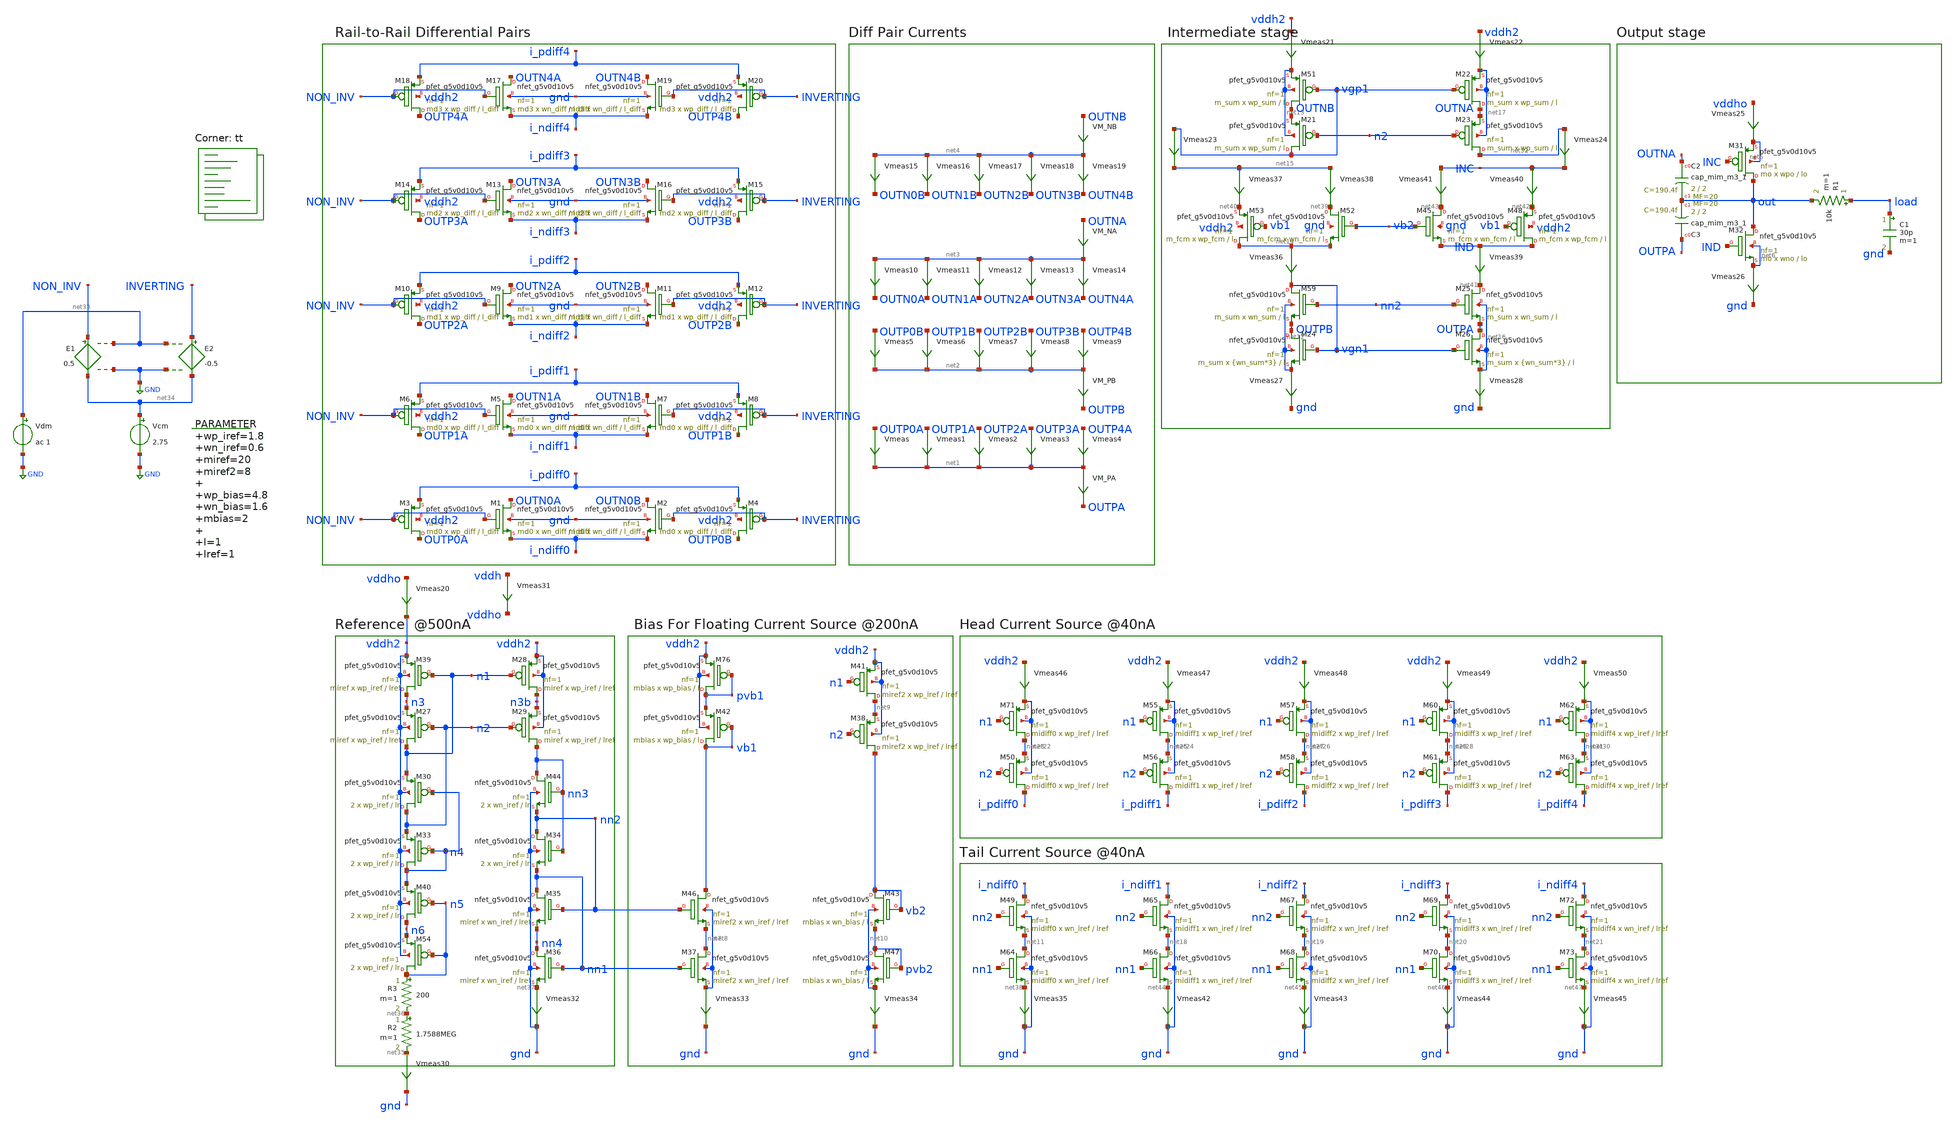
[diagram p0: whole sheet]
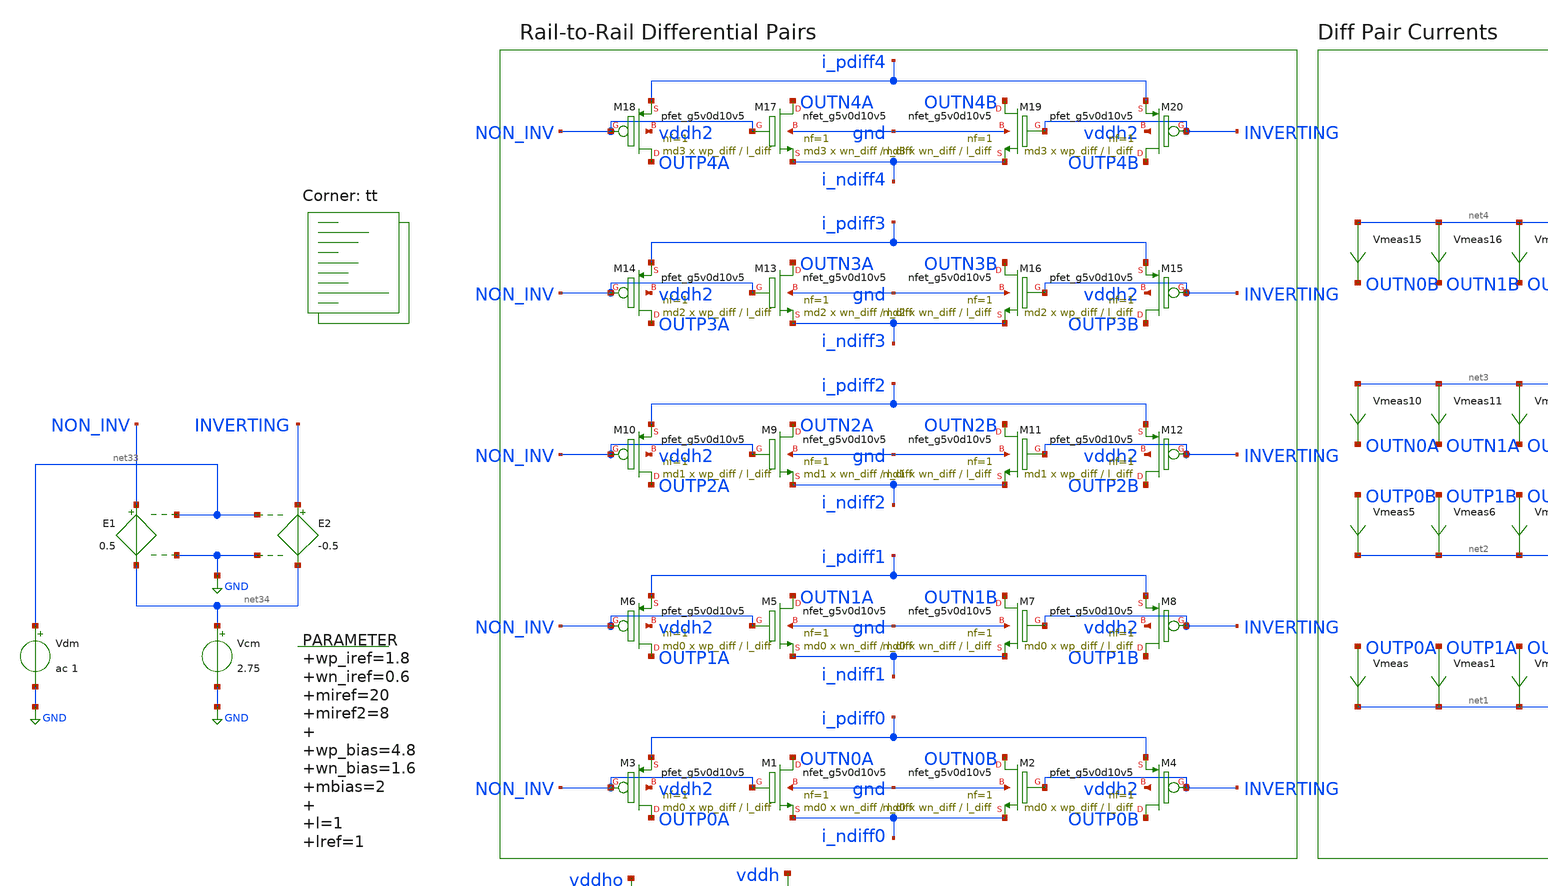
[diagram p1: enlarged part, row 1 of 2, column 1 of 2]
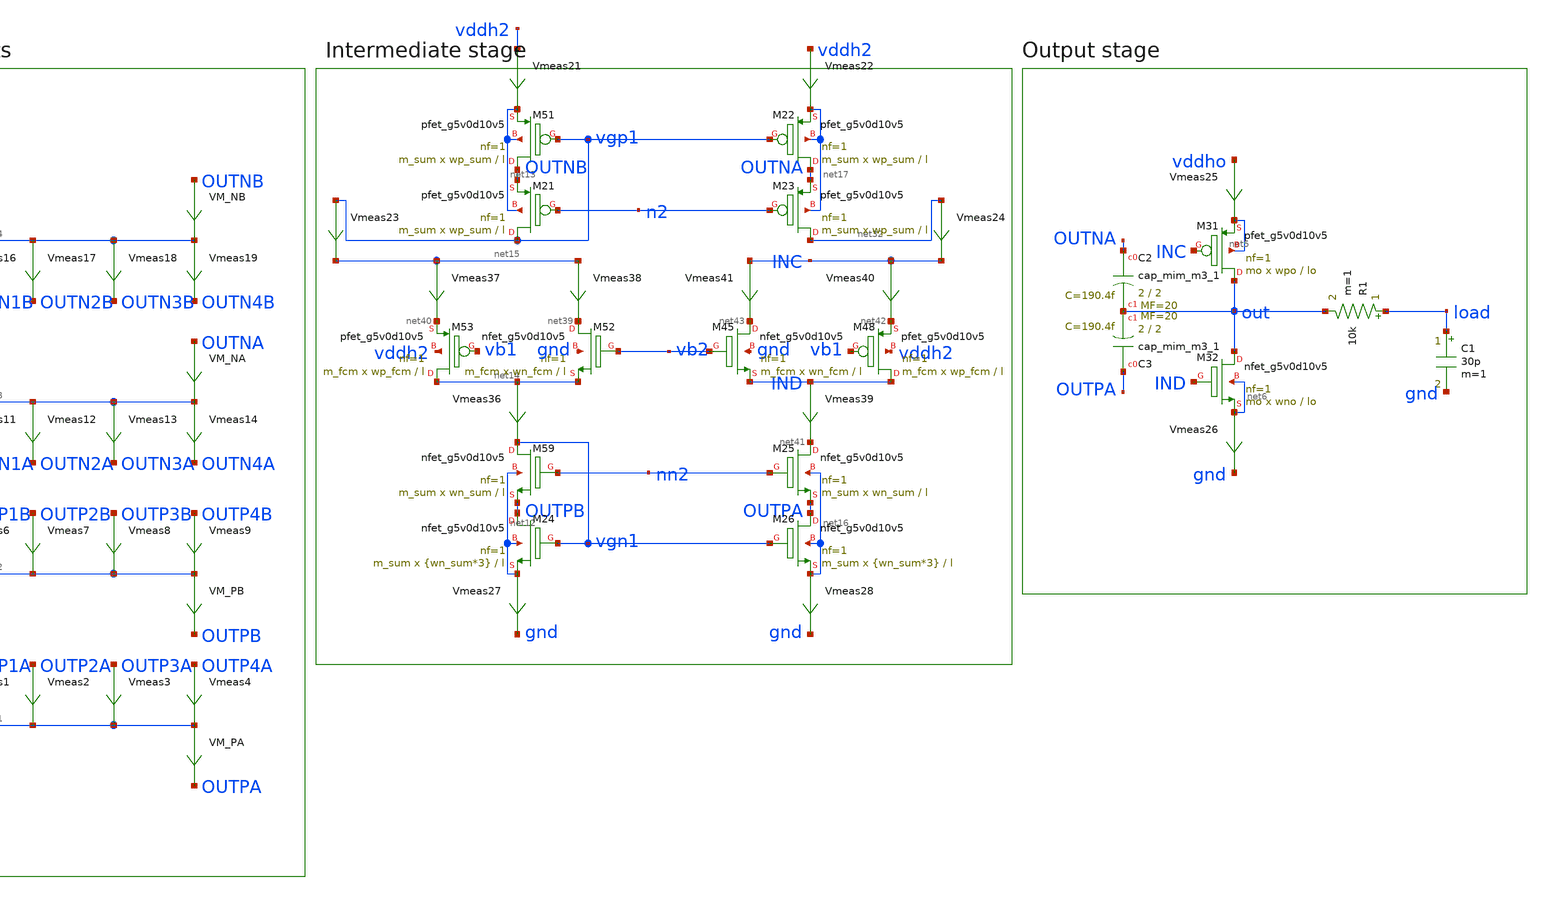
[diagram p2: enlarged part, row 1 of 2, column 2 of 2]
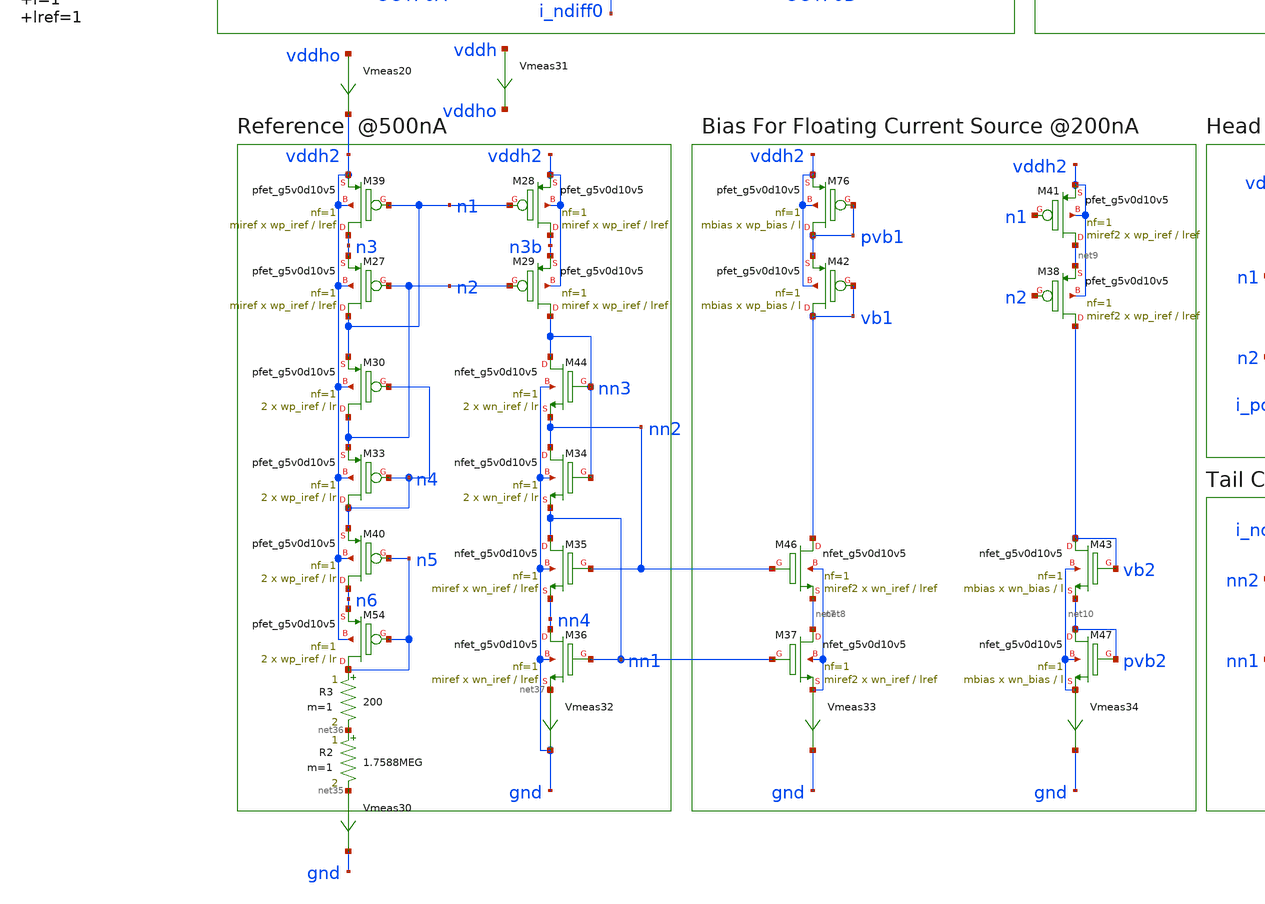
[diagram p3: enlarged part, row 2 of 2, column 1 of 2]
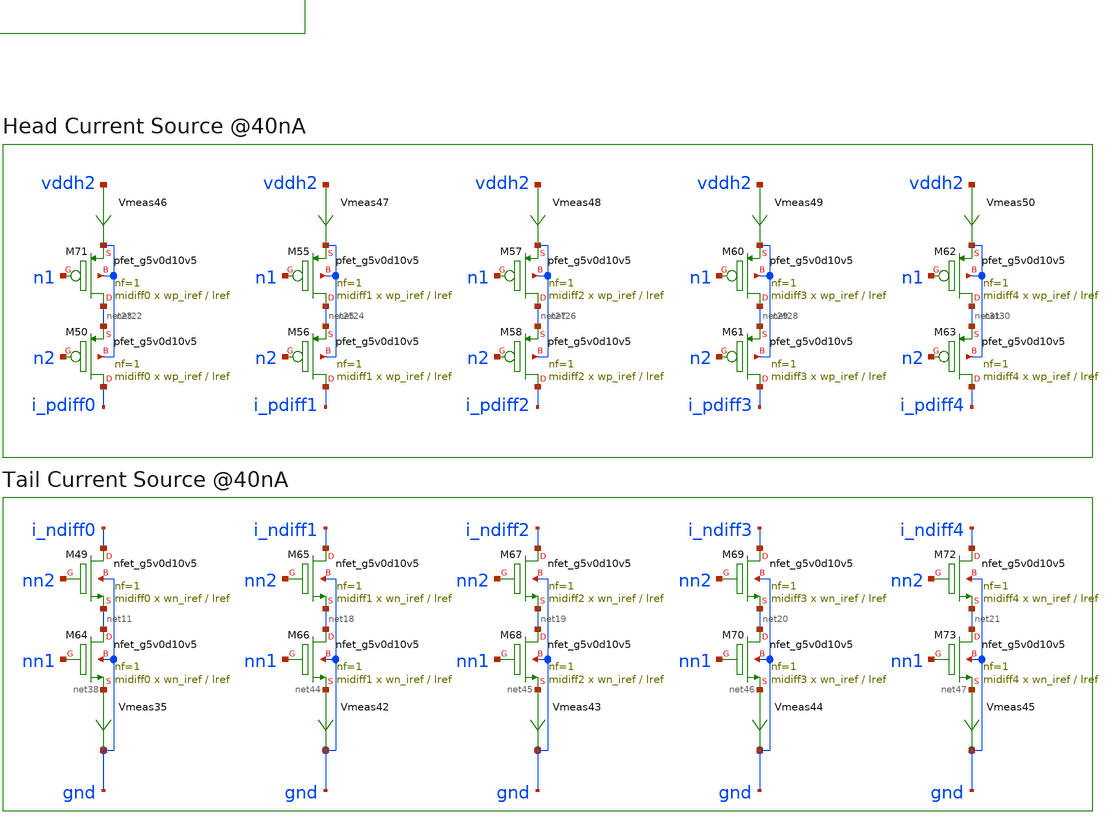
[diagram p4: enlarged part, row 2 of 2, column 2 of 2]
** sch_path: xschem/op_amp_v3-tb.sch
**.subckt op_amp_v3-tb
XM1 OUTN0A NON_INV i_ndiff0 gnd sky130_fd_pr__nfet_g5v0d10v5 L=l_diff W=wn_diff nf=1 ad='int((nf+1)/2) * W/nf * 0.29'
+ as='int((nf+2)/2) * W/nf * 0.29' pd='2*int((nf+1)/2) * (W/nf + 0.29)' ps='2*int((nf+2)/2) * (W/nf + 0.29)'
+ nrd='0.29 / W' nrs='0.29 / W' sa=0 sb=0 sd=0 mult=md0 m=md0
XM3 OUTP0A NON_INV i_pdiff0 vddh2 sky130_fd_pr__pfet_g5v0d10v5 L=l_diff W=wp_diff nf=1 ad='int((nf+1)/2) * W/nf * 0.29'
+ as='int((nf+2)/2) * W/nf * 0.29' pd='2*int((nf+1)/2) * (W/nf + 0.29)' ps='2*int((nf+2)/2) * (W/nf + 0.29)'
+ nrd='0.29 / W' nrs='0.29 / W' sa=0 sb=0 sd=0 mult=md0 m=md0
Vmeas OUTP0A net1 0
.save i(vmeas)
Vmeas1 OUTP1A net1 0
.save i(vmeas1)
Vmeas2 OUTP2A net1 0
.save i(vmeas2)
Vmeas3 OUTP3A net1 0
.save i(vmeas3)
Vmeas4 OUTP4A net1 0
.save i(vmeas4)
Vmeas5 OUTP0B net2 0
.save i(vmeas5)
Vmeas6 OUTP1B net2 0
.save i(vmeas6)
Vmeas7 OUTP2B net2 0
.save i(vmeas7)
Vmeas8 OUTP3B net2 0
.save i(vmeas8)
Vmeas9 OUTP4B net2 0
.save i(vmeas9)
Vmeas10 net3 OUTN0A 0
.save i(vmeas10)
Vmeas11 net3 OUTN1A 0
.save i(vmeas11)
Vmeas12 net3 OUTN2A 0
.save i(vmeas12)
Vmeas13 net3 OUTN3A 0
.save i(vmeas13)
Vmeas14 net3 OUTN4A 0
.save i(vmeas14)
Vmeas15 net4 OUTN0B 0
.save i(vmeas15)
Vmeas16 net4 OUTN1B 0
.save i(vmeas16)
Vmeas17 net4 OUTN2B 0
.save i(vmeas17)
Vmeas18 net4 OUTN3B 0
.save i(vmeas18)
Vmeas19 net4 OUTN4B 0
.save i(vmeas19)
XM31 out INC net5 net5 sky130_fd_pr__pfet_g5v0d10v5 L=lo W=wpo nf=1 ad='int((nf+1)/2) * W/nf * 0.29'
+ as='int((nf+2)/2) * W/nf * 0.29' pd='2*int((nf+1)/2) * (W/nf + 0.29)' ps='2*int((nf+2)/2) * (W/nf + 0.29)'
+ nrd='0.29 / W' nrs='0.29 / W' sa=0 sb=0 sd=0 mult=mo m=mo
XM32 out IND net6 net6 sky130_fd_pr__nfet_g5v0d10v5 L=lo W=wno nf=1 ad='int((nf+1)/2) * W/nf * 0.29'
+ as='int((nf+2)/2) * W/nf * 0.29' pd='2*int((nf+1)/2) * (W/nf + 0.29)' ps='2*int((nf+2)/2) * (W/nf + 0.29)'
+ nrd='0.29 / W' nrs='0.29 / W' sa=0 sb=0 sd=0 mult=mo m=mo
R1 load out 10k m=1
Vmeas25 vddho net5 0
.save i(vmeas25)
Vmeas26 net6 gnd 0
.save i(vmeas26)
C1 load gnd 30p m=1
VM_NB OUTNB net4 0
.save i(vm_nb)
VM_NA OUTNA net3 0
.save i(vm_na)
VM_PB net2 OUTPB 0
.save i(vm_pb)
VM_PA net1 OUTPA 0
.save i(vm_pa)
XM5 OUTN1A NON_INV i_ndiff1 gnd sky130_fd_pr__nfet_g5v0d10v5 L=l_diff W=wn_diff nf=1 ad='int((nf+1)/2) * W/nf * 0.29'
+ as='int((nf+2)/2) * W/nf * 0.29' pd='2*int((nf+1)/2) * (W/nf + 0.29)' ps='2*int((nf+2)/2) * (W/nf + 0.29)'
+ nrd='0.29 / W' nrs='0.29 / W' sa=0 sb=0 sd=0 mult=md0 m=md0
XM6 OUTP1A NON_INV i_pdiff1 vddh2 sky130_fd_pr__pfet_g5v0d10v5 L=l_diff W=wp_diff nf=1 ad='int((nf+1)/2) * W/nf * 0.29'
+ as='int((nf+2)/2) * W/nf * 0.29' pd='2*int((nf+1)/2) * (W/nf + 0.29)' ps='2*int((nf+2)/2) * (W/nf + 0.29)'
+ nrd='0.29 / W' nrs='0.29 / W' sa=0 sb=0 sd=0 mult=md0 m=md0
XM9 OUTN2A NON_INV i_ndiff2 gnd sky130_fd_pr__nfet_g5v0d10v5 L=l_diff W=wn_diff nf=1 ad='int((nf+1)/2) * W/nf * 0.29'
+ as='int((nf+2)/2) * W/nf * 0.29' pd='2*int((nf+1)/2) * (W/nf + 0.29)' ps='2*int((nf+2)/2) * (W/nf + 0.29)'
+ nrd='0.29 / W' nrs='0.29 / W' sa=0 sb=0 sd=0 mult=md1 m=md1
XM10 OUTP2A NON_INV i_pdiff2 vddh2 sky130_fd_pr__pfet_g5v0d10v5 L=l_diff W=wp_diff nf=1 ad='int((nf+1)/2) * W/nf * 0.29'
+ as='int((nf+2)/2) * W/nf * 0.29' pd='2*int((nf+1)/2) * (W/nf + 0.29)' ps='2*int((nf+2)/2) * (W/nf + 0.29)'
+ nrd='0.29 / W' nrs='0.29 / W' sa=0 sb=0 sd=0 mult=md1 m=md1
XM13 OUTN3A NON_INV i_ndiff3 gnd sky130_fd_pr__nfet_g5v0d10v5 L=l_diff W=wn_diff nf=1 ad='int((nf+1)/2) * W/nf * 0.29'
+ as='int((nf+2)/2) * W/nf * 0.29' pd='2*int((nf+1)/2) * (W/nf + 0.29)' ps='2*int((nf+2)/2) * (W/nf + 0.29)'
+ nrd='0.29 / W' nrs='0.29 / W' sa=0 sb=0 sd=0 mult=md2 m=md2
XM14 OUTP3A NON_INV i_pdiff3 vddh2 sky130_fd_pr__pfet_g5v0d10v5 L=l_diff W=wp_diff nf=1 ad='int((nf+1)/2) * W/nf * 0.29'
+ as='int((nf+2)/2) * W/nf * 0.29' pd='2*int((nf+1)/2) * (W/nf + 0.29)' ps='2*int((nf+2)/2) * (W/nf + 0.29)'
+ nrd='0.29 / W' nrs='0.29 / W' sa=0 sb=0 sd=0 mult=md2 m=md2
XM17 OUTN4A NON_INV i_ndiff4 gnd sky130_fd_pr__nfet_g5v0d10v5 L=l_diff W=wn_diff nf=1 ad='int((nf+1)/2) * W/nf * 0.29'
+ as='int((nf+2)/2) * W/nf * 0.29' pd='2*int((nf+1)/2) * (W/nf + 0.29)' ps='2*int((nf+2)/2) * (W/nf + 0.29)'
+ nrd='0.29 / W' nrs='0.29 / W' sa=0 sb=0 sd=0 mult=md3 m=md3
XM18 OUTP4A NON_INV i_pdiff4 vddh2 sky130_fd_pr__pfet_g5v0d10v5 L=l_diff W=wp_diff nf=1 ad='int((nf+1)/2) * W/nf * 0.29'
+ as='int((nf+2)/2) * W/nf * 0.29' pd='2*int((nf+1)/2) * (W/nf + 0.29)' ps='2*int((nf+2)/2) * (W/nf + 0.29)'
+ nrd='0.29 / W' nrs='0.29 / W' sa=0 sb=0 sd=0 mult=md3 m=md3
XM39 n3 n1 vddh2 vddh2 sky130_fd_pr__pfet_g5v0d10v5 L=lref W=wp_iref nf=1 ad='int((nf+1)/2) * W/nf * 0.29'
+ as='int((nf+2)/2) * W/nf * 0.29' pd='2*int((nf+1)/2) * (W/nf + 0.29)' ps='2*int((nf+2)/2) * (W/nf + 0.29)'
+ nrd='0.29 / W' nrs='0.29 / W' sa=0 sb=0 sd=0 mult=miref m=miref
Vmeas30 net35 gnd 0
.save i(vmeas30)
R3 n5 net36 200 m=1
Vmeas31 vddh vddho 0
.save i(vmeas31)
XM44 nn3 nn3 nn2 gnd sky130_fd_pr__nfet_g5v0d10v5 L=lr W=wn_iref nf=1 ad='int((nf+1)/2) * W/nf * 0.29'
+ as='int((nf+2)/2) * W/nf * 0.29' pd='2*int((nf+1)/2) * (W/nf + 0.29)' ps='2*int((nf+2)/2) * (W/nf + 0.29)'
+ nrd='0.29 / W' nrs='0.29 / W' sa=0 sb=0 sd=0 mult=2 m=2
Vmeas32 net37 gnd 0
.save i(vmeas32)
XM46 vb1 nn2 net7 net8 sky130_fd_pr__nfet_g5v0d10v5 L=lref W=wn_iref nf=1 ad='int((nf+1)/2) * W/nf * 0.29'
+ as='int((nf+2)/2) * W/nf * 0.29' pd='2*int((nf+1)/2) * (W/nf + 0.29)' ps='2*int((nf+2)/2) * (W/nf + 0.29)'
+ nrd='0.29 / W' nrs='0.29 / W' sa=0 sb=0 sd=0 mult=miref2 m=miref2
Vmeas33 net8 gnd 0
.save i(vmeas33)
XM47 pvb2 pvb2 net10 net10 sky130_fd_pr__nfet_g5v0d10v5 L=l W=wn_bias nf=1 ad='int((nf+1)/2) * W/nf * 0.29'
+ as='int((nf+2)/2) * W/nf * 0.29' pd='2*int((nf+1)/2) * (W/nf + 0.29)' ps='2*int((nf+2)/2) * (W/nf + 0.29)'
+ nrd='0.29 / W' nrs='0.29 / W' sa=0 sb=0 sd=0 mult=mbias m=mbias
Vmeas34 net10 gnd 0
.save i(vmeas34)
XM49 i_ndiff0 nn2 net11 gnd sky130_fd_pr__nfet_g5v0d10v5 L=lref W=wn_iref nf=1 ad='int((nf+1)/2) * W/nf * 0.29'
+ as='int((nf+2)/2) * W/nf * 0.29' pd='2*int((nf+1)/2) * (W/nf + 0.29)' ps='2*int((nf+2)/2) * (W/nf + 0.29)'
+ nrd='0.29 / W' nrs='0.29 / W' sa=0 sb=0 sd=0 mult=midiff0 m=midiff0
Vmeas35 net38 gnd 0
.save i(vmeas35)
Vmeas36 net14 vgn1 0
.save i(vmeas36)
XM51 OUTNB vgp1 net13 net13 sky130_fd_pr__pfet_g5v0d10v5 L=l W=wp_sum nf=1 ad='int((nf+1)/2) * W/nf * 0.29'
+ as='int((nf+2)/2) * W/nf * 0.29' pd='2*int((nf+1)/2) * (W/nf + 0.29)' ps='2*int((nf+2)/2) * (W/nf + 0.29)'
+ nrd='0.29 / W' nrs='0.29 / W' sa=0 sb=0 sd=0 mult=m_sum m=m_sum
XM52 net39 vb2 net14 gnd sky130_fd_pr__nfet_g5v0d10v5 L=l W=wn_fcm nf=1 ad='int((nf+1)/2) * W/nf * 0.29'
+ as='int((nf+2)/2) * W/nf * 0.29' pd='2*int((nf+1)/2) * (W/nf + 0.29)' ps='2*int((nf+2)/2) * (W/nf + 0.29)'
+ nrd='0.29 / W' nrs='0.29 / W' sa=0 sb=0 sd=0 mult=m_fcm m=m_fcm
Vmeas37 net15 net40 0
.save i(vmeas37)
Vmeas38 net15 net39 0
.save i(vmeas38)
XM53 net14 vb1 net40 vddh2 sky130_fd_pr__pfet_g5v0d10v5 L=l W=wp_fcm nf=1 ad='int((nf+1)/2) * W/nf * 0.29'
+ as='int((nf+2)/2) * W/nf * 0.29' pd='2*int((nf+1)/2) * (W/nf + 0.29)' ps='2*int((nf+2)/2) * (W/nf + 0.29)'
+ nrd='0.29 / W' nrs='0.29 / W' sa=0 sb=0 sd=0 mult=m_fcm m=m_fcm
Vmeas39 IND net41 0
.save i(vmeas39)
Vmeas40 INC net42 0
.save i(vmeas40)
Vmeas41 INC net43 0
.save i(vmeas41)
XM59 vgn1 nn2 OUTPB net12 sky130_fd_pr__nfet_g5v0d10v5 L=l W=wn_sum nf=1 ad='int((nf+1)/2) * W/nf * 0.29'
+ as='int((nf+2)/2) * W/nf * 0.29' pd='2*int((nf+1)/2) * (W/nf + 0.29)' ps='2*int((nf+2)/2) * (W/nf + 0.29)'
+ nrd='0.29 / W' nrs='0.29 / W' sa=0 sb=0 sd=0 mult=m_sum m=m_sum
Vmeas42 net44 gnd 0
.save i(vmeas42)
Vmeas43 net45 gnd 0
.save i(vmeas43)
Vmeas44 net46 gnd 0
.save i(vmeas44)
Vmeas45 net47 gnd 0
.save i(vmeas45)
XM71 net23 n1 net22 net22 sky130_fd_pr__pfet_g5v0d10v5 L=lref W=wp_iref nf=1 ad='int((nf+1)/2) * W/nf * 0.29'
+ as='int((nf+2)/2) * W/nf * 0.29' pd='2*int((nf+1)/2) * (W/nf + 0.29)' ps='2*int((nf+2)/2) * (W/nf + 0.29)'
+ nrd='0.29 / W' nrs='0.29 / W' sa=0 sb=0 sd=0 mult=midiff0 m=midiff0
Vmeas46 vddh2 net22 0
.save i(vmeas46)
XM76 pvb1 pvb1 vddh2 vddh2 sky130_fd_pr__pfet_g5v0d10v5 L=l W=wp_bias nf=1 ad='int((nf+1)/2) * W/nf * 0.29'
+ as='int((nf+2)/2) * W/nf * 0.29' pd='2*int((nf+1)/2) * (W/nf + 0.29)' ps='2*int((nf+2)/2) * (W/nf + 0.29)'
+ nrd='0.29 / W' nrs='0.29 / W' sa=0 sb=0 sd=0 mult=mbias m=mbias
Vmeas47 vddh2 net24 0
.save i(vmeas47)
Vmeas48 vddh2 net26 0
.save i(vmeas48)
Vmeas49 vddh2 net28 0
.save i(vmeas49)
Vmeas50 vddh2 net30 0
.save i(vmeas50)
.param wp_iref=1.8 wn_iref=0.6 miref=20 miref2=8 wp_bias=4.8 wn_bias=1.6 mbias=2 l=1 lref=1 lr=20
+ midiff0=2 midiff1=2 midiff2=4 midiff3=8 midiff4=16 wp_diff=3 wn_diff=1 l_diff=1 wp_sum=4.8 wn_sum=1.6 l_sum=1
+ m_sum=2 wp_fcm=wp_bias wn_fcm=wn_bias m_fcm=2 wpo=6 wno=2 lo=1 mo=2 md0=4 md1=4 md2=4 md3=4

XM21 vgp1 n2 OUTNB net13 sky130_fd_pr__pfet_g5v0d10v5 L=l W=wp_sum nf=1 ad='int((nf+1)/2) * W/nf * 0.29'
+ as='int((nf+2)/2) * W/nf * 0.29' pd='2*int((nf+1)/2) * (W/nf + 0.29)' ps='2*int((nf+2)/2) * (W/nf + 0.29)'
+ nrd='0.29 / W' nrs='0.29 / W' sa=0 sb=0 sd=0 mult=m_sum m=m_sum
XM23 net32 n2 OUTNA net17 sky130_fd_pr__pfet_g5v0d10v5 L=l W=wp_sum nf=1 ad='int((nf+1)/2) * W/nf * 0.29'
+ as='int((nf+2)/2) * W/nf * 0.29' pd='2*int((nf+1)/2) * (W/nf + 0.29)' ps='2*int((nf+2)/2) * (W/nf + 0.29)'
+ nrd='0.29 / W' nrs='0.29 / W' sa=0 sb=0 sd=0 mult=m_sum m=m_sum
XM25 net41 nn2 OUTPA net16 sky130_fd_pr__nfet_g5v0d10v5 L=l W=wn_sum nf=1 ad='int((nf+1)/2) * W/nf * 0.29'
+ as='int((nf+2)/2) * W/nf * 0.29' pd='2*int((nf+1)/2) * (W/nf + 0.29)' ps='2*int((nf+2)/2) * (W/nf + 0.29)'
+ nrd='0.29 / W' nrs='0.29 / W' sa=0 sb=0 sd=0 mult=m_sum m=m_sum
Vmeas20 vddho vddh2 0
.save i(vmeas20)
XM30 n2 n4 n1 vddh2 sky130_fd_pr__pfet_g5v0d10v5 L=lr W=wp_iref nf=1 ad='int((nf+1)/2) * W/nf * 0.29'
+ as='int((nf+2)/2) * W/nf * 0.29' pd='2*int((nf+1)/2) * (W/nf + 0.29)' ps='2*int((nf+2)/2) * (W/nf + 0.29)'
+ nrd='0.29 / W' nrs='0.29 / W' sa=0 sb=0 sd=0 mult=2 m=2
XM35 nn1 nn2 nn4 gnd sky130_fd_pr__nfet_g5v0d10v5 L=lref W=wn_iref nf=1 ad='int((nf+1)/2) * W/nf * 0.29'
+ as='int((nf+2)/2) * W/nf * 0.29' pd='2*int((nf+1)/2) * (W/nf + 0.29)' ps='2*int((nf+2)/2) * (W/nf + 0.29)'
+ nrd='0.29 / W' nrs='0.29 / W' sa=0 sb=0 sd=0 mult=miref m=miref
XM41 net9 n1 vddh2 vddh2 sky130_fd_pr__pfet_g5v0d10v5 L=lref W=wp_iref nf=1 ad='int((nf+1)/2) * W/nf * 0.29'
+ as='int((nf+2)/2) * W/nf * 0.29' pd='2*int((nf+1)/2) * (W/nf + 0.29)' ps='2*int((nf+2)/2) * (W/nf + 0.29)'
+ nrd='0.29 / W' nrs='0.29 / W' sa=0 sb=0 sd=0 mult=miref2 m=miref2
XM42 vb1 vb1 pvb1 vddh2 sky130_fd_pr__pfet_g5v0d10v5 L=l W=wp_bias nf=1 ad='int((nf+1)/2) * W/nf * 0.29'
+ as='int((nf+2)/2) * W/nf * 0.29' pd='2*int((nf+1)/2) * (W/nf + 0.29)' ps='2*int((nf+2)/2) * (W/nf + 0.29)'
+ nrd='0.29 / W' nrs='0.29 / W' sa=0 sb=0 sd=0 mult=mbias m=mbias
XM43 vb2 vb2 pvb2 net10 sky130_fd_pr__nfet_g5v0d10v5 L=l W=wn_bias nf=1 ad='int((nf+1)/2) * W/nf * 0.29'
+ as='int((nf+2)/2) * W/nf * 0.29' pd='2*int((nf+1)/2) * (W/nf + 0.29)' ps='2*int((nf+2)/2) * (W/nf + 0.29)'
+ nrd='0.29 / W' nrs='0.29 / W' sa=0 sb=0 sd=0 mult=mbias m=mbias
XM45 net43 vb2 IND gnd sky130_fd_pr__nfet_g5v0d10v5 L=l W=wn_fcm nf=1 ad='int((nf+1)/2) * W/nf * 0.29'
+ as='int((nf+2)/2) * W/nf * 0.29' pd='2*int((nf+1)/2) * (W/nf + 0.29)' ps='2*int((nf+2)/2) * (W/nf + 0.29)'
+ nrd='0.29 / W' nrs='0.29 / W' sa=0 sb=0 sd=0 mult=m_fcm m=m_fcm
XM48 IND vb1 net42 vddh2 sky130_fd_pr__pfet_g5v0d10v5 L=l W=wp_fcm nf=1 ad='int((nf+1)/2) * W/nf * 0.29'
+ as='int((nf+2)/2) * W/nf * 0.29' pd='2*int((nf+1)/2) * (W/nf + 0.29)' ps='2*int((nf+2)/2) * (W/nf + 0.29)'
+ nrd='0.29 / W' nrs='0.29 / W' sa=0 sb=0 sd=0 mult=m_fcm m=m_fcm
Vmeas21 vddh2 net13 0
.save i(vmeas21)
Vmeas22 vddh2 net17 0
.save i(vmeas22)
XM22 OUTNA vgp1 net17 net17 sky130_fd_pr__pfet_g5v0d10v5 L=l W=wp_sum nf=1 ad='int((nf+1)/2) * W/nf * 0.29'
+ as='int((nf+2)/2) * W/nf * 0.29' pd='2*int((nf+1)/2) * (W/nf + 0.29)' ps='2*int((nf+2)/2) * (W/nf + 0.29)'
+ nrd='0.29 / W' nrs='0.29 / W' sa=0 sb=0 sd=0 mult=m_sum m=m_sum
Vmeas23 vgp1 net15 0
.save i(vmeas23)
Vmeas24 net32 INC 0
.save i(vmeas24)
XM24 OUTPB vgn1 net12 net12 sky130_fd_pr__nfet_g5v0d10v5 L=l W={wn_sum*3} nf=1 ad='int((nf+1)/2) * W/nf * 0.29'
+ as='int((nf+2)/2) * W/nf * 0.29' pd='2*int((nf+1)/2) * (W/nf + 0.29)' ps='2*int((nf+2)/2) * (W/nf + 0.29)'
+ nrd='0.29 / W' nrs='0.29 / W' sa=0 sb=0 sd=0 mult=m_sum m=m_sum
Vmeas27 net12 gnd 0
.save i(vmeas27)
Vmeas28 net16 gnd 0
.save i(vmeas28)
XM27 n1 n2 n3 vddh2 sky130_fd_pr__pfet_g5v0d10v5 L=lref W=wp_iref nf=1 ad='int((nf+1)/2) * W/nf * 0.29'
+ as='int((nf+2)/2) * W/nf * 0.29' pd='2*int((nf+1)/2) * (W/nf + 0.29)' ps='2*int((nf+2)/2) * (W/nf + 0.29)'
+ nrd='0.29 / W' nrs='0.29 / W' sa=0 sb=0 sd=0 mult=miref m=miref
XM28 n3b n1 vddh2 vddh2 sky130_fd_pr__pfet_g5v0d10v5 L=lref W=wp_iref nf=1 ad='int((nf+1)/2) * W/nf * 0.29'
+ as='int((nf+2)/2) * W/nf * 0.29' pd='2*int((nf+1)/2) * (W/nf + 0.29)' ps='2*int((nf+2)/2) * (W/nf + 0.29)'
+ nrd='0.29 / W' nrs='0.29 / W' sa=0 sb=0 sd=0 mult=miref m=miref
XM29 nn3 n2 n3b vddh2 sky130_fd_pr__pfet_g5v0d10v5 L=lref W=wp_iref nf=1 ad='int((nf+1)/2) * W/nf * 0.29'
+ as='int((nf+2)/2) * W/nf * 0.29' pd='2*int((nf+1)/2) * (W/nf + 0.29)' ps='2*int((nf+2)/2) * (W/nf + 0.29)'
+ nrd='0.29 / W' nrs='0.29 / W' sa=0 sb=0 sd=0 mult=miref m=miref
XM36 nn4 nn1 net37 gnd sky130_fd_pr__nfet_g5v0d10v5 L=lref W=wn_iref nf=1 ad='int((nf+1)/2) * W/nf * 0.29'
+ as='int((nf+2)/2) * W/nf * 0.29' pd='2*int((nf+1)/2) * (W/nf + 0.29)' ps='2*int((nf+2)/2) * (W/nf + 0.29)'
+ nrd='0.29 / W' nrs='0.29 / W' sa=0 sb=0 sd=0 mult=miref m=miref
XM37 net7 nn1 net8 net8 sky130_fd_pr__nfet_g5v0d10v5 L=lref W=wn_iref nf=1 ad='int((nf+1)/2) * W/nf * 0.29'
+ as='int((nf+2)/2) * W/nf * 0.29' pd='2*int((nf+1)/2) * (W/nf + 0.29)' ps='2*int((nf+2)/2) * (W/nf + 0.29)'
+ nrd='0.29 / W' nrs='0.29 / W' sa=0 sb=0 sd=0 mult=miref2 m=miref2
XM38 vb2 n2 net9 vddh2 sky130_fd_pr__pfet_g5v0d10v5 L=lref W=wp_iref nf=1 ad='int((nf+1)/2) * W/nf * 0.29'
+ as='int((nf+2)/2) * W/nf * 0.29' pd='2*int((nf+1)/2) * (W/nf + 0.29)' ps='2*int((nf+2)/2) * (W/nf + 0.29)'
+ nrd='0.29 / W' nrs='0.29 / W' sa=0 sb=0 sd=0 mult=miref2 m=miref2
XM50 i_pdiff0 n2 net23 net22 sky130_fd_pr__pfet_g5v0d10v5 L=lref W=wp_iref nf=1 ad='int((nf+1)/2) * W/nf * 0.29'
+ as='int((nf+2)/2) * W/nf * 0.29' pd='2*int((nf+1)/2) * (W/nf + 0.29)' ps='2*int((nf+2)/2) * (W/nf + 0.29)'
+ nrd='0.29 / W' nrs='0.29 / W' sa=0 sb=0 sd=0 mult=midiff0 m=midiff0
XM55 net25 n1 net24 net24 sky130_fd_pr__pfet_g5v0d10v5 L=lref W=wp_iref nf=1 ad='int((nf+1)/2) * W/nf * 0.29'
+ as='int((nf+2)/2) * W/nf * 0.29' pd='2*int((nf+1)/2) * (W/nf + 0.29)' ps='2*int((nf+2)/2) * (W/nf + 0.29)'
+ nrd='0.29 / W' nrs='0.29 / W' sa=0 sb=0 sd=0 mult=midiff1 m=midiff1
XM56 i_pdiff1 n2 net25 net24 sky130_fd_pr__pfet_g5v0d10v5 L=lref W=wp_iref nf=1 ad='int((nf+1)/2) * W/nf * 0.29'
+ as='int((nf+2)/2) * W/nf * 0.29' pd='2*int((nf+1)/2) * (W/nf + 0.29)' ps='2*int((nf+2)/2) * (W/nf + 0.29)'
+ nrd='0.29 / W' nrs='0.29 / W' sa=0 sb=0 sd=0 mult=midiff1 m=midiff1
XM57 net27 n1 net26 net26 sky130_fd_pr__pfet_g5v0d10v5 L=lref W=wp_iref nf=1 ad='int((nf+1)/2) * W/nf * 0.29'
+ as='int((nf+2)/2) * W/nf * 0.29' pd='2*int((nf+1)/2) * (W/nf + 0.29)' ps='2*int((nf+2)/2) * (W/nf + 0.29)'
+ nrd='0.29 / W' nrs='0.29 / W' sa=0 sb=0 sd=0 mult=midiff2 m=midiff2
XM58 i_pdiff2 n2 net27 net26 sky130_fd_pr__pfet_g5v0d10v5 L=lref W=wp_iref nf=1 ad='int((nf+1)/2) * W/nf * 0.29'
+ as='int((nf+2)/2) * W/nf * 0.29' pd='2*int((nf+1)/2) * (W/nf + 0.29)' ps='2*int((nf+2)/2) * (W/nf + 0.29)'
+ nrd='0.29 / W' nrs='0.29 / W' sa=0 sb=0 sd=0 mult=midiff2 m=midiff2
XM60 net29 n1 net28 net28 sky130_fd_pr__pfet_g5v0d10v5 L=lref W=wp_iref nf=1 ad='int((nf+1)/2) * W/nf * 0.29'
+ as='int((nf+2)/2) * W/nf * 0.29' pd='2*int((nf+1)/2) * (W/nf + 0.29)' ps='2*int((nf+2)/2) * (W/nf + 0.29)'
+ nrd='0.29 / W' nrs='0.29 / W' sa=0 sb=0 sd=0 mult=midiff3 m=midiff3
XM61 i_pdiff3 n2 net29 net28 sky130_fd_pr__pfet_g5v0d10v5 L=lref W=wp_iref nf=1 ad='int((nf+1)/2) * W/nf * 0.29'
+ as='int((nf+2)/2) * W/nf * 0.29' pd='2*int((nf+1)/2) * (W/nf + 0.29)' ps='2*int((nf+2)/2) * (W/nf + 0.29)'
+ nrd='0.29 / W' nrs='0.29 / W' sa=0 sb=0 sd=0 mult=midiff3 m=midiff3
XM62 net31 n1 net30 net30 sky130_fd_pr__pfet_g5v0d10v5 L=lref W=wp_iref nf=1 ad='int((nf+1)/2) * W/nf * 0.29'
+ as='int((nf+2)/2) * W/nf * 0.29' pd='2*int((nf+1)/2) * (W/nf + 0.29)' ps='2*int((nf+2)/2) * (W/nf + 0.29)'
+ nrd='0.29 / W' nrs='0.29 / W' sa=0 sb=0 sd=0 mult=midiff4 m=midiff4
XM63 i_pdiff4 n2 net31 net30 sky130_fd_pr__pfet_g5v0d10v5 L=lref W=wp_iref nf=1 ad='int((nf+1)/2) * W/nf * 0.29'
+ as='int((nf+2)/2) * W/nf * 0.29' pd='2*int((nf+1)/2) * (W/nf + 0.29)' ps='2*int((nf+2)/2) * (W/nf + 0.29)'
+ nrd='0.29 / W' nrs='0.29 / W' sa=0 sb=0 sd=0 mult=midiff4 m=midiff4
XM64 net11 nn1 net38 gnd sky130_fd_pr__nfet_g5v0d10v5 L=lref W=wn_iref nf=1 ad='int((nf+1)/2) * W/nf * 0.29'
+ as='int((nf+2)/2) * W/nf * 0.29' pd='2*int((nf+1)/2) * (W/nf + 0.29)' ps='2*int((nf+2)/2) * (W/nf + 0.29)'
+ nrd='0.29 / W' nrs='0.29 / W' sa=0 sb=0 sd=0 mult=midiff0 m=midiff0
XM65 i_ndiff1 nn2 net18 gnd sky130_fd_pr__nfet_g5v0d10v5 L=lref W=wn_iref nf=1 ad='int((nf+1)/2) * W/nf * 0.29'
+ as='int((nf+2)/2) * W/nf * 0.29' pd='2*int((nf+1)/2) * (W/nf + 0.29)' ps='2*int((nf+2)/2) * (W/nf + 0.29)'
+ nrd='0.29 / W' nrs='0.29 / W' sa=0 sb=0 sd=0 mult=midiff1 m=midiff1
XM66 net18 nn1 net44 gnd sky130_fd_pr__nfet_g5v0d10v5 L=lref W=wn_iref nf=1 ad='int((nf+1)/2) * W/nf * 0.29'
+ as='int((nf+2)/2) * W/nf * 0.29' pd='2*int((nf+1)/2) * (W/nf + 0.29)' ps='2*int((nf+2)/2) * (W/nf + 0.29)'
+ nrd='0.29 / W' nrs='0.29 / W' sa=0 sb=0 sd=0 mult=midiff1 m=midiff1
XM67 i_ndiff2 nn2 net19 gnd sky130_fd_pr__nfet_g5v0d10v5 L=lref W=wn_iref nf=1 ad='int((nf+1)/2) * W/nf * 0.29'
+ as='int((nf+2)/2) * W/nf * 0.29' pd='2*int((nf+1)/2) * (W/nf + 0.29)' ps='2*int((nf+2)/2) * (W/nf + 0.29)'
+ nrd='0.29 / W' nrs='0.29 / W' sa=0 sb=0 sd=0 mult=midiff2 m=midiff2
XM68 net19 nn1 net45 gnd sky130_fd_pr__nfet_g5v0d10v5 L=lref W=wn_iref nf=1 ad='int((nf+1)/2) * W/nf * 0.29'
+ as='int((nf+2)/2) * W/nf * 0.29' pd='2*int((nf+1)/2) * (W/nf + 0.29)' ps='2*int((nf+2)/2) * (W/nf + 0.29)'
+ nrd='0.29 / W' nrs='0.29 / W' sa=0 sb=0 sd=0 mult=midiff2 m=midiff2
XM69 i_ndiff3 nn2 net20 gnd sky130_fd_pr__nfet_g5v0d10v5 L=lref W=wn_iref nf=1 ad='int((nf+1)/2) * W/nf * 0.29'
+ as='int((nf+2)/2) * W/nf * 0.29' pd='2*int((nf+1)/2) * (W/nf + 0.29)' ps='2*int((nf+2)/2) * (W/nf + 0.29)'
+ nrd='0.29 / W' nrs='0.29 / W' sa=0 sb=0 sd=0 mult=midiff3 m=midiff3
XM70 net20 nn1 net46 gnd sky130_fd_pr__nfet_g5v0d10v5 L=lref W=wn_iref nf=1 ad='int((nf+1)/2) * W/nf * 0.29'
+ as='int((nf+2)/2) * W/nf * 0.29' pd='2*int((nf+1)/2) * (W/nf + 0.29)' ps='2*int((nf+2)/2) * (W/nf + 0.29)'
+ nrd='0.29 / W' nrs='0.29 / W' sa=0 sb=0 sd=0 mult=midiff3 m=midiff3
XM72 i_ndiff4 nn2 net21 gnd sky130_fd_pr__nfet_g5v0d10v5 L=lref W=wn_iref nf=1 ad='int((nf+1)/2) * W/nf * 0.29'
+ as='int((nf+2)/2) * W/nf * 0.29' pd='2*int((nf+1)/2) * (W/nf + 0.29)' ps='2*int((nf+2)/2) * (W/nf + 0.29)'
+ nrd='0.29 / W' nrs='0.29 / W' sa=0 sb=0 sd=0 mult=midiff4 m=midiff4
XM73 net21 nn1 net47 gnd sky130_fd_pr__nfet_g5v0d10v5 L=lref W=wn_iref nf=1 ad='int((nf+1)/2) * W/nf * 0.29'
+ as='int((nf+2)/2) * W/nf * 0.29' pd='2*int((nf+1)/2) * (W/nf + 0.29)' ps='2*int((nf+2)/2) * (W/nf + 0.29)'
+ nrd='0.29 / W' nrs='0.29 / W' sa=0 sb=0 sd=0 mult=midiff4 m=midiff4
XM33 n4 n4 n2 vddh2 sky130_fd_pr__pfet_g5v0d10v5 L=lr W=wp_iref nf=1 ad='int((nf+1)/2) * W/nf * 0.29'
+ as='int((nf+2)/2) * W/nf * 0.29' pd='2*int((nf+1)/2) * (W/nf + 0.29)' ps='2*int((nf+2)/2) * (W/nf + 0.29)'
+ nrd='0.29 / W' nrs='0.29 / W' sa=0 sb=0 sd=0 mult=2 m=2
XM40 n6 n5 n4 vddh2 sky130_fd_pr__pfet_g5v0d10v5 L=lr W=wp_iref nf=1 ad='int((nf+1)/2) * W/nf * 0.29'
+ as='int((nf+2)/2) * W/nf * 0.29' pd='2*int((nf+1)/2) * (W/nf + 0.29)' ps='2*int((nf+2)/2) * (W/nf + 0.29)'
+ nrd='0.29 / W' nrs='0.29 / W' sa=0 sb=0 sd=0 mult=2 m=2
XM54 n5 n5 n6 vddh2 sky130_fd_pr__pfet_g5v0d10v5 L=lr W=wp_iref nf=1 ad='int((nf+1)/2) * W/nf * 0.29'
+ as='int((nf+2)/2) * W/nf * 0.29' pd='2*int((nf+1)/2) * (W/nf + 0.29)' ps='2*int((nf+2)/2) * (W/nf + 0.29)'
+ nrd='0.29 / W' nrs='0.29 / W' sa=0 sb=0 sd=0 mult=2 m=2
XM34 nn2 nn3 nn1 gnd sky130_fd_pr__nfet_g5v0d10v5 L=lr W=wn_iref nf=1 ad='int((nf+1)/2) * W/nf * 0.29'
+ as='int((nf+2)/2) * W/nf * 0.29' pd='2*int((nf+1)/2) * (W/nf + 0.29)' ps='2*int((nf+2)/2) * (W/nf + 0.29)'
+ nrd='0.29 / W' nrs='0.29 / W' sa=0 sb=0 sd=0 mult=2 m=2
XM26 OUTPA vgn1 net16 net16 sky130_fd_pr__nfet_g5v0d10v5 L=l W={wn_sum*3} nf=1 ad='int((nf+1)/2) * W/nf * 0.29'
+ as='int((nf+2)/2) * W/nf * 0.29' pd='2*int((nf+1)/2) * (W/nf + 0.29)' ps='2*int((nf+2)/2) * (W/nf + 0.29)'
+ nrd='0.29 / W' nrs='0.29 / W' sa=0 sb=0 sd=0 mult=m_sum m=m_sum
XC2 OUTNA out sky130_fd_pr__cap_mim_m3_1 W=2 L=2 MF=20 m=20
XC3 OUTPA out sky130_fd_pr__cap_mim_m3_1 W=2 L=2 MF=20 m=20
E1 NON_INV net34 net33 GND 0.5
E2 INVERTING net34 net33 GND -0.5
Vdm net33 GND ac 1
Vcm net34 GND 2.75
R2 net36 net35 1.7588MEG m=1
XM4 OUTP0B INVERTING i_pdiff0 vddh2 sky130_fd_pr__pfet_g5v0d10v5 L=l_diff W=wp_diff nf=1 ad='int((nf+1)/2) * W/nf * 0.29'
+ as='int((nf+2)/2) * W/nf * 0.29' pd='2*int((nf+1)/2) * (W/nf + 0.29)' ps='2*int((nf+2)/2) * (W/nf + 0.29)'
+ nrd='0.29 / W' nrs='0.29 / W' sa=0 sb=0 sd=0 mult=md0 m=md0
XM2 OUTN0B INVERTING i_ndiff0 gnd sky130_fd_pr__nfet_g5v0d10v5 L=l_diff W=wn_diff nf=1 ad='int((nf+1)/2) * W/nf * 0.29'
+ as='int((nf+2)/2) * W/nf * 0.29' pd='2*int((nf+1)/2) * (W/nf + 0.29)' ps='2*int((nf+2)/2) * (W/nf + 0.29)'
+ nrd='0.29 / W' nrs='0.29 / W' sa=0 sb=0 sd=0 mult=md0 m=md0
XM8 OUTP1B INVERTING i_pdiff1 vddh2 sky130_fd_pr__pfet_g5v0d10v5 L=l_diff W=wp_diff nf=1 ad='int((nf+1)/2) * W/nf * 0.29'
+ as='int((nf+2)/2) * W/nf * 0.29' pd='2*int((nf+1)/2) * (W/nf + 0.29)' ps='2*int((nf+2)/2) * (W/nf + 0.29)'
+ nrd='0.29 / W' nrs='0.29 / W' sa=0 sb=0 sd=0 mult=md0 m=md0
XM7 OUTN1B INVERTING i_ndiff1 gnd sky130_fd_pr__nfet_g5v0d10v5 L=l_diff W=wn_diff nf=1 ad='int((nf+1)/2) * W/nf * 0.29'
+ as='int((nf+2)/2) * W/nf * 0.29' pd='2*int((nf+1)/2) * (W/nf + 0.29)' ps='2*int((nf+2)/2) * (W/nf + 0.29)'
+ nrd='0.29 / W' nrs='0.29 / W' sa=0 sb=0 sd=0 mult=md0 m=md0
XM12 OUTP2B INVERTING i_pdiff2 vddh2 sky130_fd_pr__pfet_g5v0d10v5 L=l_diff W=wp_diff nf=1 ad='int((nf+1)/2) * W/nf * 0.29'
+ as='int((nf+2)/2) * W/nf * 0.29' pd='2*int((nf+1)/2) * (W/nf + 0.29)' ps='2*int((nf+2)/2) * (W/nf + 0.29)'
+ nrd='0.29 / W' nrs='0.29 / W' sa=0 sb=0 sd=0 mult=md1 m=md1
XM11 OUTN2B INVERTING i_ndiff2 gnd sky130_fd_pr__nfet_g5v0d10v5 L=l_diff W=wn_diff nf=1 ad='int((nf+1)/2) * W/nf * 0.29'
+ as='int((nf+2)/2) * W/nf * 0.29' pd='2*int((nf+1)/2) * (W/nf + 0.29)' ps='2*int((nf+2)/2) * (W/nf + 0.29)'
+ nrd='0.29 / W' nrs='0.29 / W' sa=0 sb=0 sd=0 mult=md1 m=md1
XM15 OUTP3B INVERTING i_pdiff3 vddh2 sky130_fd_pr__pfet_g5v0d10v5 L=l_diff W=wp_diff nf=1 ad='int((nf+1)/2) * W/nf * 0.29'
+ as='int((nf+2)/2) * W/nf * 0.29' pd='2*int((nf+1)/2) * (W/nf + 0.29)' ps='2*int((nf+2)/2) * (W/nf + 0.29)'
+ nrd='0.29 / W' nrs='0.29 / W' sa=0 sb=0 sd=0 mult=md2 m=md2
XM16 OUTN3B INVERTING i_ndiff3 gnd sky130_fd_pr__nfet_g5v0d10v5 L=l_diff W=wn_diff nf=1 ad='int((nf+1)/2) * W/nf * 0.29'
+ as='int((nf+2)/2) * W/nf * 0.29' pd='2*int((nf+1)/2) * (W/nf + 0.29)' ps='2*int((nf+2)/2) * (W/nf + 0.29)'
+ nrd='0.29 / W' nrs='0.29 / W' sa=0 sb=0 sd=0 mult=md2 m=md2
XM20 OUTP4B INVERTING i_pdiff4 vddh2 sky130_fd_pr__pfet_g5v0d10v5 L=l_diff W=wp_diff nf=1 ad='int((nf+1)/2) * W/nf * 0.29'
+ as='int((nf+2)/2) * W/nf * 0.29' pd='2*int((nf+1)/2) * (W/nf + 0.29)' ps='2*int((nf+2)/2) * (W/nf + 0.29)'
+ nrd='0.29 / W' nrs='0.29 / W' sa=0 sb=0 sd=0 mult=md3 m=md3
XM19 OUTN4B INVERTING i_ndiff4 gnd sky130_fd_pr__nfet_g5v0d10v5 L=l_diff W=wn_diff nf=1 ad='int((nf+1)/2) * W/nf * 0.29'
+ as='int((nf+2)/2) * W/nf * 0.29' pd='2*int((nf+1)/2) * (W/nf + 0.29)' ps='2*int((nf+2)/2) * (W/nf + 0.29)'
+ nrd='0.29 / W' nrs='0.29 / W' sa=0 sb=0 sd=0 mult=md3 m=md3
**** begin user architecture code
.lib $::SKYWATER_MODELS/sky130.lib.spice tt



  .option wnflag=1
  .option safecurrents
  .option solver=klu
  ********************Static Voltage Sources***************************
  Vddh vddh gnd dc 5.5

  *vn2 vn2 gnd 3.3
  *vnn2 vnn2 gnd 1.8
  *vb1 vb1 gnd 3.4
  *vb2 vb2 gnd 1.74
  *vina ina gnd sin({5.5/2} {5.5/2} 100k)
  *vinb inb gnd sin({5.5/2} {-5.5/2} 100k)

  .param vin_val=4.661
  *vin0 in[0] gnd dc vin_val
  *vin1 in[1] gnd dc vin_val
  *vin2 in[2] gnd dc vin_val
  *vin3 in[3] gnd dc vin_val
  *vin4 in[4] gnd dc vin_val
  ********************Dynamic Voltage Sources***************************
  *******Calculation**********
  .param base_f=100e3 base_t={1/base_f} base_th={base_t/2} base_d={base_th}
  .param b0_th={base_th} b0_t={b0_th*2}
  .param b1_th={b0_th*2} b1_t={b1_th*2}
  .param b2_th={b1_th*2} b2_t={b2_th*2}
  .param b3_th={b2_th*2} b3_t={b3_th*2}
  *******Signals**********
  .param vh=1.162 vl=1.044
  *vin0 in[0] gnd dc pulse(5.5 0 {base_d} 1n 1n {b0_th} {b0_t})
  *vin0 in[0] gnd dc 2.75
  vin0 in[0] gnd dc vl
  Vin1 in[1] gnd pulse({vh} {vl} {base_d} 1n 1n {b0_th} {b0_t})
  Vin2 in[2] gnd pulse({vh} {vl} {base_d} 1n 1n {b1_th} {b1_t})
  Vin3 in[3] gnd pulse({vh} {vl} {base_d} 1n 1n {b2_th} {b2_t})
  Vin4 in[4] gnd pulse({vh} {vl} {base_d} 1n 1n {b3_th} {b3_t})
  ********************Simulation Commands*****************************
  .control
     reset
     save all
     set num_threads=8
     *save inc ind out load
     *tran 10n 100u
     *dc vin0 -1 6.5 0.01
     *dc R2 100k 500k 1k

     ac dec 100 1 1e9
     let difference=v(inc)-v(ind)
     let vout_mag =abs(v(out))
     let vout_phase_margin = phase(v(out))*180/pi + 180
     meas ac Aol find vout_mag at = 10
     meas ac UGF when vout_mag=1 fall=1
     meas ac PM find vout_phase_margin when vout_mag=1

     save difference
     write op_amp_v3-tb.raw
     set wr_vecnames
     set wr_singlescale
     wrdata $THESIS_WS/simulations/op_amp_v3-tb.txt out load
     set appendwrite
*    quit 0
  .endc



**** end user architecture code
**.ends
.GLOBAL GND
.end
